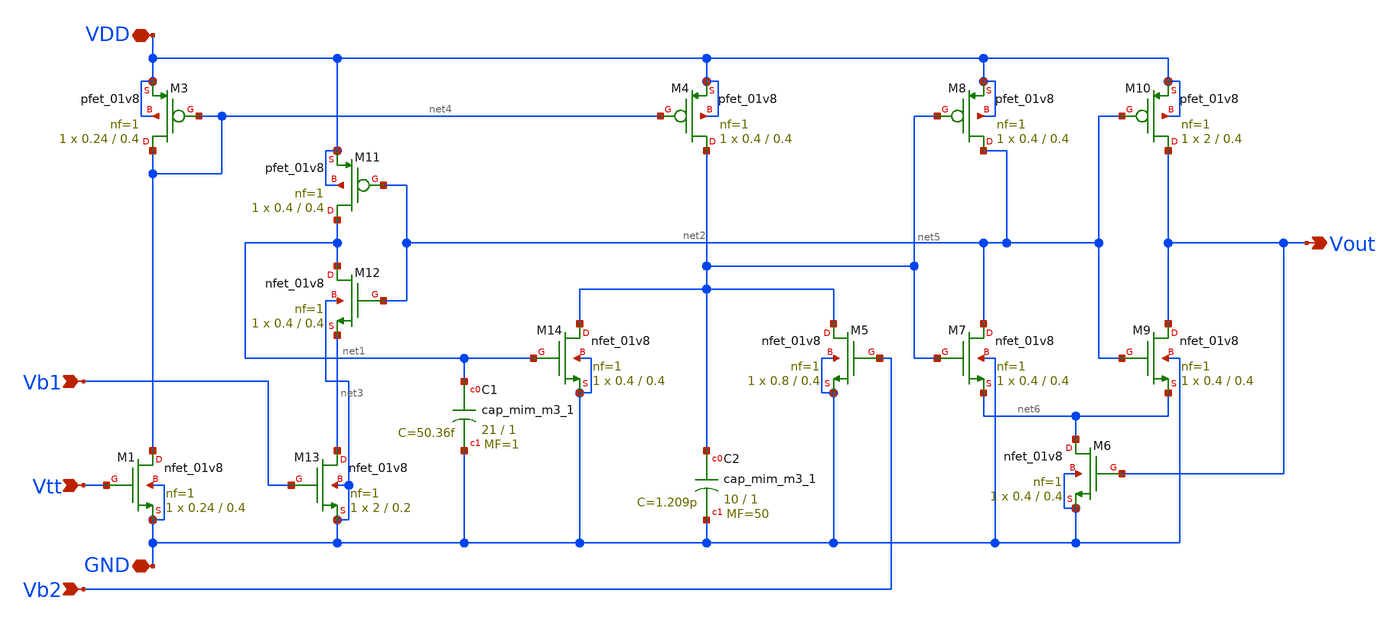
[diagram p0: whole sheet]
** sch_path: LIF_neuron/LIF_neuron_Vohra.sch
**.subckt LIF_neuron_Vohra Vtt GND Vb1 Vb2 VDD Vout
*.ipin Vtt
*.iopin GND
*.ipin Vb1
*.ipin Vb2
*.iopin VDD
*.opin Vout
XM1 net4 Vtt GND GND sky130_fd_pr__nfet_01v8 L=0.4 W=0.24 nf=1 ad='int((nf+1)/2) * W/nf * 0.29' as='int((nf+2)/2) * W/nf * 0.29'
+ pd='2*int((nf+1)/2) * (W/nf + 0.29)' ps='2*int((nf+2)/2) * (W/nf + 0.29)' nrd='0.29 / W' nrs='0.29 / W'
+ sa=0 sb=0 sd=0 mult=1 m=1
XM3 net4 net4 VDD VDD sky130_fd_pr__pfet_01v8 L=0.4 W=0.24 nf=1 ad='int((nf+1)/2) * W/nf * 0.29' as='int((nf+2)/2) * W/nf * 0.29'
+ pd='2*int((nf+1)/2) * (W/nf + 0.29)' ps='2*int((nf+2)/2) * (W/nf + 0.29)' nrd='0.29 / W' nrs='0.29 / W'
+ sa=0 sb=0 sd=0 mult=1 m=1
XM13 net3 Vb1 GND GND sky130_fd_pr__nfet_01v8 L=0.2 W=2 nf=1 ad='int((nf+1)/2) * W/nf * 0.29' as='int((nf+2)/2) * W/nf * 0.29'
+ pd='2*int((nf+1)/2) * (W/nf + 0.29)' ps='2*int((nf+2)/2) * (W/nf + 0.29)' nrd='0.29 / W' nrs='0.29 / W'
+ sa=0 sb=0 sd=0 mult=1 m=1
XM12 net1 net2 net3 GND sky130_fd_pr__nfet_01v8 L=0.4 W=0.4 nf=1 ad='int((nf+1)/2) * W/nf * 0.29' as='int((nf+2)/2) * W/nf * 0.29'
+ pd='2*int((nf+1)/2) * (W/nf + 0.29)' ps='2*int((nf+2)/2) * (W/nf + 0.29)' nrd='0.29 / W' nrs='0.29 / W'
+ sa=0 sb=0 sd=0 mult=1 m=1
XM11 net1 net2 VDD VDD sky130_fd_pr__pfet_01v8 L=0.4 W=0.4 nf=1 ad='int((nf+1)/2) * W/nf * 0.29' as='int((nf+2)/2) * W/nf * 0.29'
+ pd='2*int((nf+1)/2) * (W/nf + 0.29)' ps='2*int((nf+2)/2) * (W/nf + 0.29)' nrd='0.29 / W' nrs='0.29 / W'
+ sa=0 sb=0 sd=0 mult=1 m=1
XC1 net1 GND sky130_fd_pr__cap_mim_m3_1 W=21 L=1 MF=1 m=1
XM14 net5 net1 GND GND sky130_fd_pr__nfet_01v8 L=0.4 W=0.4 nf=1 ad='int((nf+1)/2) * W/nf * 0.29' as='int((nf+2)/2) * W/nf * 0.29'
+ pd='2*int((nf+1)/2) * (W/nf + 0.29)' ps='2*int((nf+2)/2) * (W/nf + 0.29)' nrd='0.29 / W' nrs='0.29 / W'
+ sa=0 sb=0 sd=0 mult=1 m=1
XM4 net5 net4 VDD VDD sky130_fd_pr__pfet_01v8 L=0.4 W=0.4 nf=1 ad='int((nf+1)/2) * W/nf * 0.29' as='int((nf+2)/2) * W/nf * 0.29'
+ pd='2*int((nf+1)/2) * (W/nf + 0.29)' ps='2*int((nf+2)/2) * (W/nf + 0.29)' nrd='0.29 / W' nrs='0.29 / W'
+ sa=0 sb=0 sd=0 mult=1 m=1
XC2 net5 GND sky130_fd_pr__cap_mim_m3_1 W=10 L=1 MF=50 m=50
XM5 net5 Vb2 GND GND sky130_fd_pr__nfet_01v8 L=0.4 W=0.8 nf=1 ad='int((nf+1)/2) * W/nf * 0.29' as='int((nf+2)/2) * W/nf * 0.29'
+ pd='2*int((nf+1)/2) * (W/nf + 0.29)' ps='2*int((nf+2)/2) * (W/nf + 0.29)' nrd='0.29 / W' nrs='0.29 / W'
+ sa=0 sb=0 sd=0 mult=1 m=1
XM6 net6 Vout GND GND sky130_fd_pr__nfet_01v8 L=0.4 W=0.4 nf=1 ad='int((nf+1)/2) * W/nf * 0.29' as='int((nf+2)/2) * W/nf * 0.29'
+ pd='2*int((nf+1)/2) * (W/nf + 0.29)' ps='2*int((nf+2)/2) * (W/nf + 0.29)' nrd='0.29 / W' nrs='0.29 / W'
+ sa=0 sb=0 sd=0 mult=1 m=1
XM7 net2 net5 net6 GND sky130_fd_pr__nfet_01v8 L=0.4 W=0.4 nf=1 ad='int((nf+1)/2) * W/nf * 0.29' as='int((nf+2)/2) * W/nf * 0.29'
+ pd='2*int((nf+1)/2) * (W/nf + 0.29)' ps='2*int((nf+2)/2) * (W/nf + 0.29)' nrd='0.29 / W' nrs='0.29 / W'
+ sa=0 sb=0 sd=0 mult=1 m=1
XM8 net2 net5 VDD VDD sky130_fd_pr__pfet_01v8 L=0.4 W=0.4 nf=1 ad='int((nf+1)/2) * W/nf * 0.29' as='int((nf+2)/2) * W/nf * 0.29'
+ pd='2*int((nf+1)/2) * (W/nf + 0.29)' ps='2*int((nf+2)/2) * (W/nf + 0.29)' nrd='0.29 / W' nrs='0.29 / W'
+ sa=0 sb=0 sd=0 mult=1 m=1
XM9 Vout net2 net6 GND sky130_fd_pr__nfet_01v8 L=0.4 W=0.4 nf=1 ad='int((nf+1)/2) * W/nf * 0.29' as='int((nf+2)/2) * W/nf * 0.29'
+ pd='2*int((nf+1)/2) * (W/nf + 0.29)' ps='2*int((nf+2)/2) * (W/nf + 0.29)' nrd='0.29 / W' nrs='0.29 / W'
+ sa=0 sb=0 sd=0 mult=1 m=1
XM10 Vout net2 VDD VDD sky130_fd_pr__pfet_01v8 L=0.4 W=2 nf=1 ad='int((nf+1)/2) * W/nf * 0.29' as='int((nf+2)/2) * W/nf * 0.29'
+ pd='2*int((nf+1)/2) * (W/nf + 0.29)' ps='2*int((nf+2)/2) * (W/nf + 0.29)' nrd='0.29 / W' nrs='0.29 / W'
+ sa=0 sb=0 sd=0 mult=1 m=1
**.ends
.end
